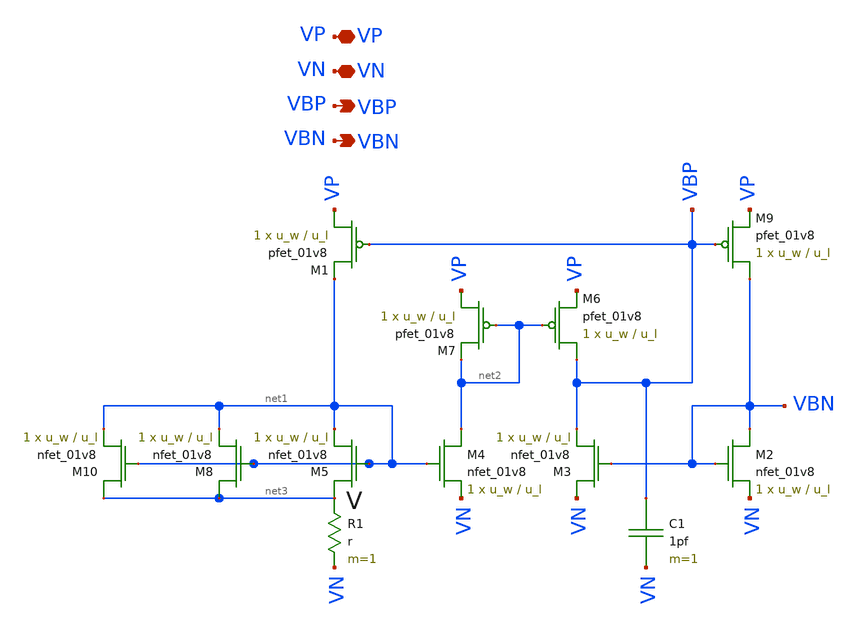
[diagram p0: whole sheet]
** sch_path: lib/analog/schematic/bias_gen.sch
**.subckt bias_gen VN VP VBP VBN
*.iopin VN
*.iopin VP
*.opin VBP
*.opin VBN
R1 net3 VN r m=1
XM5 net3 net1 net1 GND sky130_fd_pr__nfet_01v8 L=u_l W=u_w nf=1 ad='int((nf+1)/2) * W/nf * 0.29' as='int((nf+2)/2) * W/nf * 0.29'
+ pd='2*int((nf+1)/2) * (W/nf + 0.29)' ps='2*int((nf+2)/2) * (W/nf + 0.29)' nrd='0.29 / W' nrs='0.29 / W'
+ sa=0 sb=0 sd=0 mult=1 m=1
XM2 VBN VBN VN GND sky130_fd_pr__nfet_01v8 L=u_l W=u_w nf=1 ad='int((nf+1)/2) * W/nf * 0.29' as='int((nf+2)/2) * W/nf * 0.29'
+ pd='2*int((nf+1)/2) * (W/nf + 0.29)' ps='2*int((nf+2)/2) * (W/nf + 0.29)' nrd='0.29 / W' nrs='0.29 / W'
+ sa=0 sb=0 sd=0 mult=1 m=1
XM9 VBN VBP VP VDD sky130_fd_pr__pfet_01v8 L=u_l W=u_w nf=1 ad='int((nf+1)/2) * W/nf * 0.29' as='int((nf+2)/2) * W/nf * 0.29'
+ pd='2*int((nf+1)/2) * (W/nf + 0.29)' ps='2*int((nf+2)/2) * (W/nf + 0.29)' nrd='0.29 / W' nrs='0.29 / W'
+ sa=0 sb=0 sd=0 mult=1 m=1
XM1 VP VBP net1 VDD sky130_fd_pr__pfet_01v8 L=u_l W=u_w nf=1 ad='int((nf+1)/2) * W/nf * 0.29' as='int((nf+2)/2) * W/nf * 0.29'
+ pd='2*int((nf+1)/2) * (W/nf + 0.29)' ps='2*int((nf+2)/2) * (W/nf + 0.29)' nrd='0.29 / W' nrs='0.29 / W'
+ sa=0 sb=0 sd=0 mult=1 m=1
XM3 VN VBN VBP GND sky130_fd_pr__nfet_01v8 L=u_l W=u_w nf=1 ad='int((nf+1)/2) * W/nf * 0.29' as='int((nf+2)/2) * W/nf * 0.29'
+ pd='2*int((nf+1)/2) * (W/nf + 0.29)' ps='2*int((nf+2)/2) * (W/nf + 0.29)' nrd='0.29 / W' nrs='0.29 / W'
+ sa=0 sb=0 sd=0 mult=1 m=1
XM4 net2 net1 VN GND sky130_fd_pr__nfet_01v8 L=u_l W=u_w nf=1 ad='int((nf+1)/2) * W/nf * 0.29' as='int((nf+2)/2) * W/nf * 0.29'
+ pd='2*int((nf+1)/2) * (W/nf + 0.29)' ps='2*int((nf+2)/2) * (W/nf + 0.29)' nrd='0.29 / W' nrs='0.29 / W'
+ sa=0 sb=0 sd=0 mult=1 m=1
XM6 VBP net2 VP VDD sky130_fd_pr__pfet_01v8 L=u_l W=u_w nf=1 ad='int((nf+1)/2) * W/nf * 0.29' as='int((nf+2)/2) * W/nf * 0.29'
+ pd='2*int((nf+1)/2) * (W/nf + 0.29)' ps='2*int((nf+2)/2) * (W/nf + 0.29)' nrd='0.29 / W' nrs='0.29 / W'
+ sa=0 sb=0 sd=0 mult=1 m=1
XM7 VP net2 net2 VDD sky130_fd_pr__pfet_01v8 L=u_l W=u_w nf=1 ad='int((nf+1)/2) * W/nf * 0.29' as='int((nf+2)/2) * W/nf * 0.29'
+ pd='2*int((nf+1)/2) * (W/nf + 0.29)' ps='2*int((nf+2)/2) * (W/nf + 0.29)' nrd='0.29 / W' nrs='0.29 / W'
+ sa=0 sb=0 sd=0 mult=1 m=1
C1 VBP VN 1pf m=1
XM8 net3 net1 net1 GND sky130_fd_pr__nfet_01v8 L=u_l W=u_w nf=1 ad='int((nf+1)/2) * W/nf * 0.29' as='int((nf+2)/2) * W/nf * 0.29'
+ pd='2*int((nf+1)/2) * (W/nf + 0.29)' ps='2*int((nf+2)/2) * (W/nf + 0.29)' nrd='0.29 / W' nrs='0.29 / W'
+ sa=0 sb=0 sd=0 mult=1 m=1
XM10 net3 net1 net1 GND sky130_fd_pr__nfet_01v8 L=u_l W=u_w nf=1 ad='int((nf+1)/2) * W/nf * 0.29' as='int((nf+2)/2) * W/nf * 0.29'
+ pd='2*int((nf+1)/2) * (W/nf + 0.29)' ps='2*int((nf+2)/2) * (W/nf + 0.29)' nrd='0.29 / W' nrs='0.29 / W'
+ sa=0 sb=0 sd=0 mult=1 m=1
**.ends
.end
